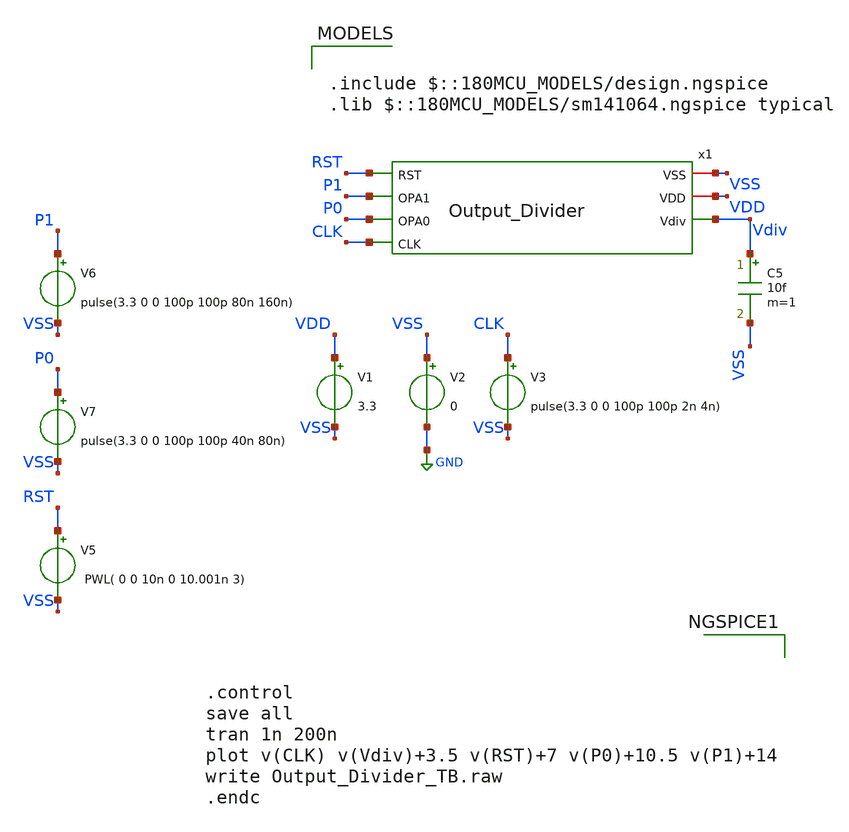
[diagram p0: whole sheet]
** sch_path: Clock_Generator_PAKISTAN_02/xschem/Output_Divider_TB.sch
**.subckt Output_Divider_TB
V1 VDD VSS 3.3
V2 VSS GND 0
V3 CLK VSS pulse(3.3 0 0 100p 100p 2n 4n)
C5 Vdiv VSS 10f m=1
V5 RST VSS PWL( 0 0 10n 0 10.001n 3)
V6 P1 VSS pulse(3.3 0 0 100p 100p 80n 160n)
V7 P0 VSS pulse(3.3 0 0 100p 100p 40n 80n)
x1 VSS VDD RST Vdiv P1 P0 CLK Output_Divider
**** begin user architecture code

.include $::180MCU_MODELS/design.ngspice
.lib $::180MCU_MODELS/sm141064.ngspice typical




.control
save all
tran 1n 200n
plot v(CLK) v(Vdiv)+3.5 v(RST)+7 v(P0)+10.5 v(P1)+14
write Output_Divider_TB.raw
.endc


**** end user architecture code
**.ends
.GLOBAL GND
.end
